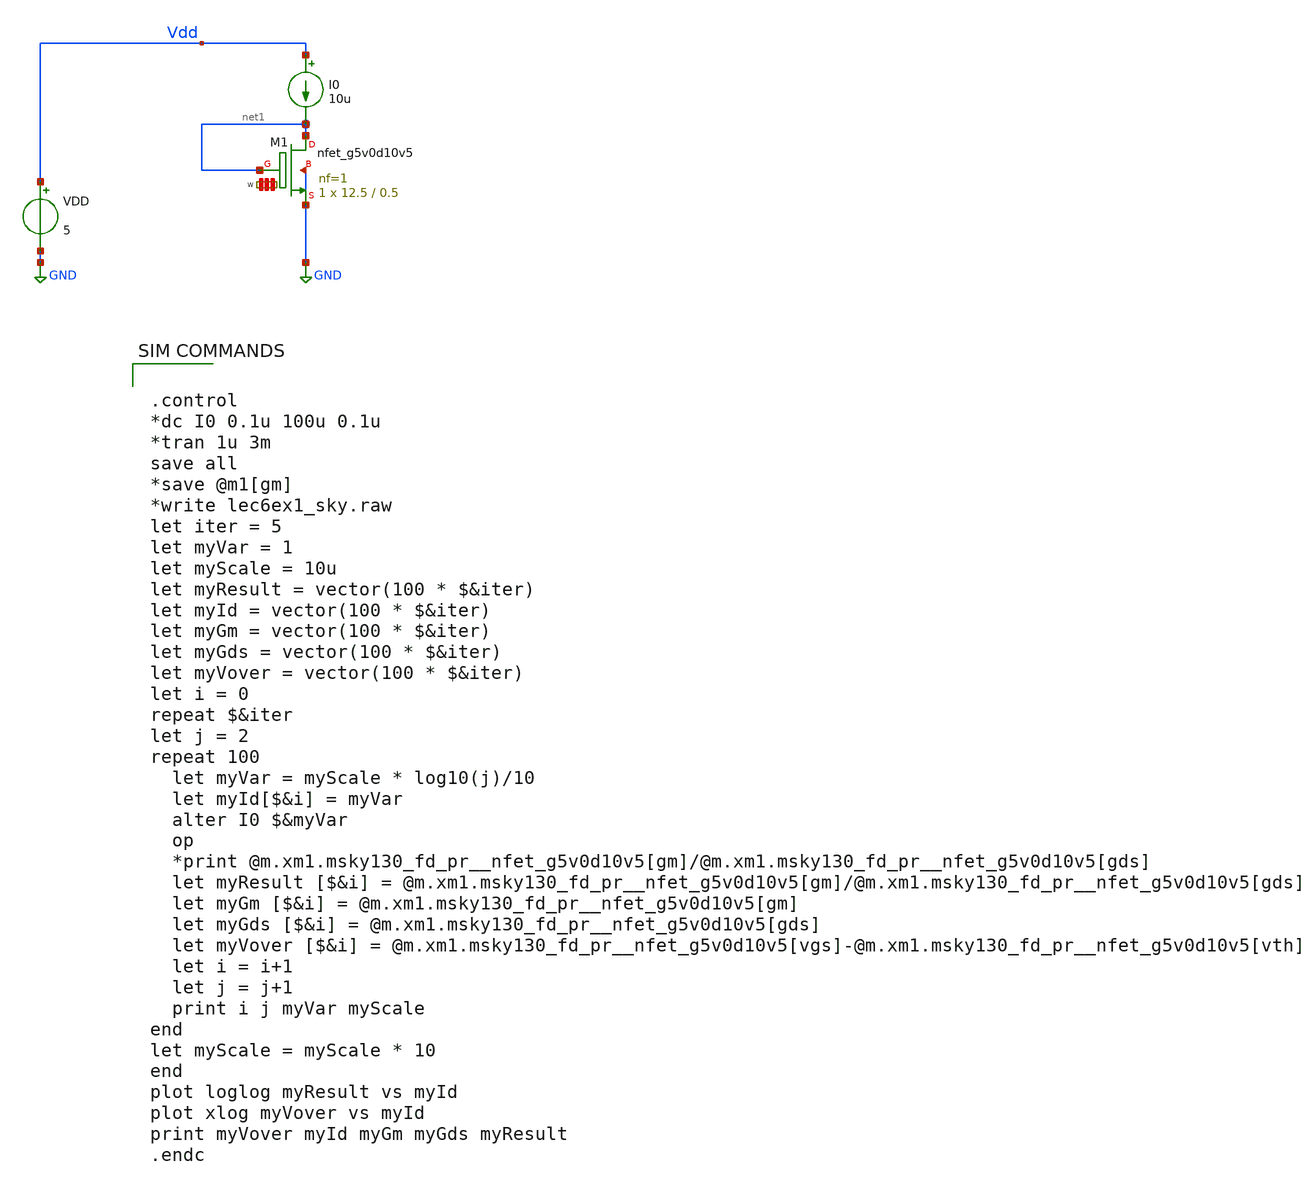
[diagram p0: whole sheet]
** sch_path: lec6ex1_sky.sch
**.subckt lec6ex1_sky
VDD Vdd GND 5
I0 Vdd net1 10u
XM1 net1 net1 GND GND sky130_fd_pr__nfet_g5v0d10v5 L=0.5 W='12.5 * 1 ' nf=1 ad='int((nf+1)/2) * W / nf * 0.29'
+ as='int((nf+2)/2) * W / nf * 0.29' pd='2*int((nf+1)/2) * (W / nf + 0.29)' ps='2*int((nf+2)/2) * (W / nf + 0.29)'
+ nrd='0.29 / W ' nrs='0.29 / W ' sa=0 sb=0 sd=0 mult=1 m=1
**** begin user architecture code


.control
*dc I0 0.1u 100u 0.1u
*tran 1u 3m
save all
*save @m1[gm]
*write lec6ex1_sky.raw
let iter = 5
let myVar = 1
let myScale = 10u
let myResult = vector(100 * $&iter)
let myId = vector(100 * $&iter)
let myGm = vector(100 * $&iter)
let myGds = vector(100 * $&iter)
let myVover = vector(100 * $&iter)
let i = 0
repeat $&iter
let j = 2
repeat 100
  let myVar = myScale * log10(j)/10
  let myId[$&i] = myVar
  alter I0 $&myVar
  op
  *print @m.xm1.msky130_fd_pr__nfet_g5v0d10v5[gm]/@m.xm1.msky130_fd_pr__nfet_g5v0d10v5[gds]
  let myResult [$&i] =
+ @m.xm1.msky130_fd_pr__nfet_g5v0d10v5[gm]/@m.xm1.msky130_fd_pr__nfet_g5v0d10v5[gds]
  let myGm [$&i] = @m.xm1.msky130_fd_pr__nfet_g5v0d10v5[gm]
  let myGds [$&i] = @m.xm1.msky130_fd_pr__nfet_g5v0d10v5[gds]
  let myVover [$&i] =
+ @m.xm1.msky130_fd_pr__nfet_g5v0d10v5[vgs]-@m.xm1.msky130_fd_pr__nfet_g5v0d10v5[vth]
  let i = i+1
  let j = j+1
  print i j myVar myScale
end
let myScale = myScale * 10
end
plot loglog myResult vs myId
plot xlog myVover vs myId
print myVover myId myGm myGds myResult
.endc



** opencircuitdesign pdks install
.lib $::SKYWATER_MODELS/sky130.lib.spice tt


**** end user architecture code
**.ends
.GLOBAL GND
.end
